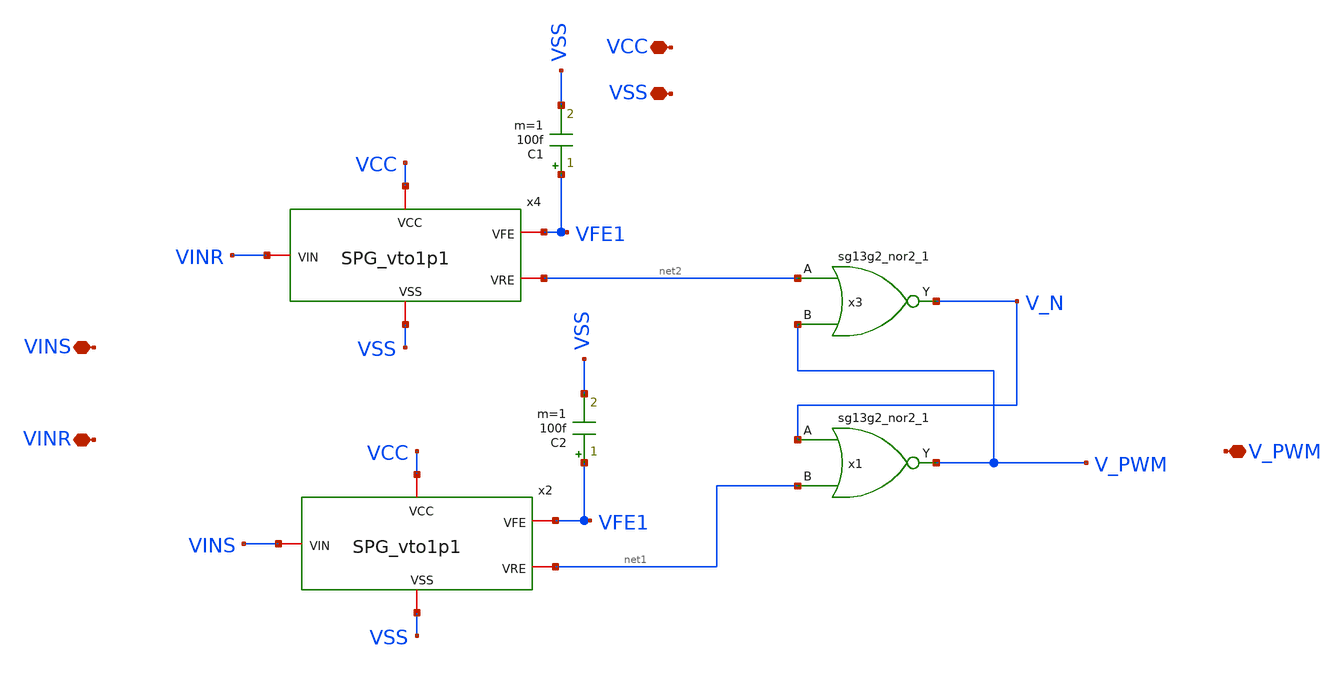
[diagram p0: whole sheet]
** sch_path: ChipUSM_AnalogTrack24/PD/PD_vto1p1.sch
* IHP-GmbH/IHP-Open-PDK/ihp-sg13g2/libs.tech/xschem/sg13g2_stdcells/sg13g2_inv_2.sch:
* Copyright 2023 IHP PDK Authors
* Licensed under the Apache License, Version 2.0 (the "License");
**.subckt PD_vto1p1 V_PWM VCC VSS VINS VINR
*.iopin V_PWM
*.iopin VCC
*.iopin VSS
*.iopin VINS
*.iopin VINR
x3 V_N net2 V_PWM VCC VSS sg13g2_nor2_1
x1 V_PWM V_N net1 VCC VSS sg13g2_nor2_1
C2 VFE1 VSS 100f m=1
C1 VFE1 VSS 100f m=1
x4 VCC VSS VFE1 VINR net2 SPG_vto1p1
x2 VCC VSS VFE1 VINS net1 SPG_vto1p1
**.ends

* expanding   symbol:  sg13g2_stdcells/sg13g2_nor2_1.sym # of pins=3
** sym_path: sg13g2_stdcells/sg13g2_nor2_1.sym
** sch_path: sg13g2_stdcells/sg13g2_nor2_1.sch
.subckt sg13g2_nor2_1 Y A B VDD VSS
*.opin Y
*.ipin B
*.ipin A
*.iopin VDD
*.iopin VSS
XM1 Y A VSS VSS sg13_lv_nmos w=740.00n l=130.00n ng=1 m=1 mm_ok=1
XM2 Y B VSS VSS sg13_lv_nmos w=740.00n l=130.00n ng=1 m=1 mm_ok=1
XM3 net1 A VDD VDD sg13_lv_pmos w=1.12u l=130.00n ng=1 m=1 mm_ok=1
XM4 Y B net1 VDD sg13_lv_pmos w=1.12u l=130.00n ng=1 m=1 mm_ok=1
.ends


* expanding   symbol:  ../SPG/SPG_vto1p1.sym # of pins=5
** sym_path: ../SPG/SPG_vto1p1.sym
** sch_path: ../SPG/SPG_vto1p1.sch
.subckt SPG_vto1p1 VCC VSS VFE VIN VRE
*.iopin VIN
*.iopin VFE
*.iopin VRE
*.iopin VCC
*.iopin VSS
x1 dly8 dly7 VCC VSS sg13g2_inv_1
x2 net2 predly VCC VSS sg13g2_inv_1
x3 predly net3 VCC VSS sg13g2_inv_1
x4 net1 dly8 VCC VSS sg13g2_inv_1
x5 net3 VIN VCC VSS sg13g2_inv_2
x6 V_gatein predly VCC VSS sg13g2_inv_8
x7 VFE net2 dly8 VCC VSS sg13g2_and2_2
x8 VRE net1 predly VCC VSS sg13g2_and2_2
x9 VCC VSS V_gatein dly7 large_delay_vto1p1
.ends


* expanding   symbol:  sg13g2_stdcells/sg13g2_inv_1.sym # of pins=2
** sym_path: sg13g2_stdcells/sg13g2_inv_1.sym
** sch_path: sg13g2_stdcells/sg13g2_inv_1.sch
.subckt sg13g2_inv_1 Y A VDD VSS
*.opin Y
*.ipin A
*.iopin VDD
*.iopin VSS
XM1 Y A VSS VSS sg13_lv_nmos w=740.00n l=130.00n ng=1 m=1 mm_ok=1
XM2 Y A VDD VDD sg13_lv_pmos w=1.12u l=130.00n ng=1 m=1 mm_ok=1
.ends


* expanding   symbol:  sg13g2_stdcells/sg13g2_inv_2.sym # of pins=2
** sym_path: sg13g2_stdcells/sg13g2_inv_2.sym
** sch_path: sg13g2_stdcells/sg13g2_inv_2.sch
.subckt sg13g2_inv_2 Y A VDD VSS
*.opin Y
*.ipin A
*.iopin VDD
*.iopin VSS
XM1 Y A VSS VSS sg13_lv_nmos w=1.48u l=130.00n ng=2 m=1 mm_ok=1
XM2 Y A VDD VDD sg13_lv_pmos w=2.24u l=130.00n ng=2 m=1 mm_ok=1
.ends


* expanding   symbol:  sg13g2_stdcells/sg13g2_inv_8.sym # of pins=2
** sym_path: sg13g2_stdcells/sg13g2_inv_8.sym
** sch_path: sg13g2_stdcells/sg13g2_inv_8.sch
.subckt sg13g2_inv_8 Y A VDD VSS
*.opin Y
*.ipin A
*.iopin VDD
*.iopin VSS
XM1 Y A VSS VSS sg13_lv_nmos w=5.92u l=130.00n ng=8 m=1 mm_ok=1
XM2 Y A VDD VDD sg13_lv_pmos w=8.96u l=130.00n ng=8 m=1 mm_ok=1
.ends


* expanding   symbol:  sg13g2_stdcells/sg13g2_and2_2.sym # of pins=3
** sym_path: sg13g2_stdcells/sg13g2_and2_2.sym
** sch_path: sg13g2_stdcells/sg13g2_and2_2.sch
.subckt sg13g2_and2_2 X A B VDD VSS
*.ipin A
*.ipin B
*.opin X
*.iopin VDD
*.iopin VSS
XM1 net1 A net2 VSS sg13_lv_nmos w=640.00n l=130.00n ng=1 m=1 mm_ok=1
XM2 net2 B VSS VSS sg13_lv_nmos w=640.00n l=130.00n ng=1 m=1 mm_ok=1
XM3 X net1 VSS VSS sg13_lv_nmos w=1.48u l=130.00n ng=2 m=1 mm_ok=1
XM4 net1 B VDD VDD sg13_lv_pmos w=840.00n l=130.00n ng=1 m=1 mm_ok=1
XM5 net1 A VDD VDD sg13_lv_pmos w=840.00n l=130.00n ng=1 m=1 mm_ok=1
XM6 X net1 VDD VDD sg13_lv_pmos w=2.24u l=130.00n ng=2 m=1 mm_ok=1
.ends


* expanding   symbol:  ../large_delay/large_delay_vto1p1.sym # of pins=4
** sym_path: ../large_delay/large_delay_vto1p1.sym
** sch_path: ../large_delay/large_delay_vto1p1.sch
.subckt large_delay_vto1p1 VCC VSS VIN VOUT
*.iopin VIN
*.iopin VOUT
*.iopin VCC
*.iopin VSS
x1[0] n2 VIN VCC VSS sg13g2_dlygate4sd3_1
x1[1] n3 n2 VCC VSS sg13g2_dlygate4sd3_1
x1[2] n4 n3 VCC VSS sg13g2_dlygate4sd3_1
x1[3] n5 n4 VCC VSS sg13g2_dlygate4sd3_1
x1[4] VOUT n5 VCC VSS sg13g2_dlygate4sd3_1
.ends


* expanding   symbol:  sg13g2_stdcells/sg13g2_dlygate4sd3_1.sym # of pins=2
** sym_path: sg13g2_stdcells/sg13g2_dlygate4sd3_1.sym
** sch_path: sg13g2_stdcells/sg13g2_dlygate4sd3_1.sch
.subckt sg13g2_dlygate4sd3_1 X A VDD VSS
*.ipin A
*.opin X
*.iopin VDD
*.iopin VSS
XM1 net3 A VSS VSS sg13_lv_nmos w=420.00n l=130.00n ng=1 m=1 mm_ok=1
XM2 net1 net3 VSS VSS sg13_lv_nmos w=420.00n l=500.0n ng=1 m=1 mm_ok=1
XM3 net2 net1 VSS VSS sg13_lv_nmos w=420.00n l=500.0n ng=1 m=1 mm_ok=1
XM4 X net2 VSS VSS sg13_lv_nmos w=740.00n l=130.00n ng=1 m=1 mm_ok=1
XM5 net3 A VDD VDD sg13_lv_pmos w=420.00n l=130.00n ng=1 m=1 mm_ok=1
XM6 net1 net3 VDD VDD sg13_lv_pmos w=1.000u l=500.0n ng=1 m=1 mm_ok=1
XM7 net2 net1 VDD VDD sg13_lv_pmos w=1.000u l=500.0n ng=1 m=1 mm_ok=1
XM8 X net2 VDD VDD sg13_lv_pmos w=1.12u l=130.00n ng=1 m=1 mm_ok=1
.ends

.end
